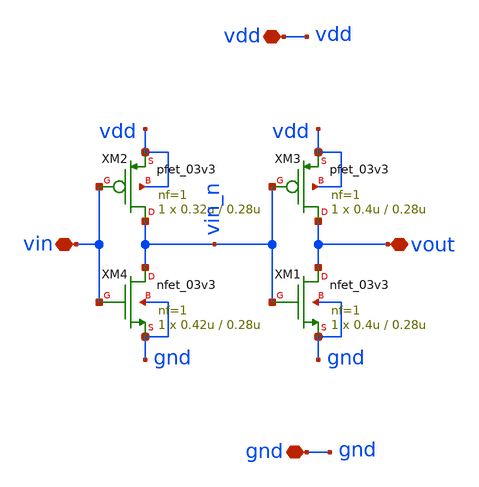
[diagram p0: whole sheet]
** sch_path: designs/libs/core_buffer/buffer.sch
**.subckt buffer vdd gnd vout vin
*.iopin vdd
*.iopin gnd
*.iopin vout
*.iopin vin
XM2 vin_n vin vdd vdd pfet_03v3 L=0.28u W=0.32u nf=1 ad='int((nf+1)/2) * W/nf * 0.18u' as='int((nf+2)/2) * W/nf * 0.18u'
+ pd='2*int((nf+1)/2) * (W/nf + 0.18u)' ps='2*int((nf+2)/2) * (W/nf + 0.18u)' nrd='0.18u / W' nrs='0.18u / W'
+ sa=0 sb=0 sd=0 m=1
XM4 vin_n vin gnd gnd nfet_03v3 L=0.28u W=0.42u nf=1 ad='int((nf+1)/2) * W/nf * 0.18u' as='int((nf+2)/2) * W/nf * 0.18u'
+ pd='2*int((nf+1)/2) * (W/nf + 0.18u)' ps='2*int((nf+2)/2) * (W/nf + 0.18u)' nrd='0.18u / W' nrs='0.18u / W'
+ sa=0 sb=0 sd=0 m=1
XM1 vout vin_n gnd gnd nfet_03v3 L=0.28u W=0.4u nf=1 ad='int((nf+1)/2) * W/nf * 0.18u' as='int((nf+2)/2) * W/nf * 0.18u'
+ pd='2*int((nf+1)/2) * (W/nf + 0.18u)' ps='2*int((nf+2)/2) * (W/nf + 0.18u)' nrd='0.18u / W' nrs='0.18u / W'
+ sa=0 sb=0 sd=0 m=1
XM3 vout vin_n vdd vdd pfet_03v3 L=0.28u W=0.4u nf=1 ad='int((nf+1)/2) * W/nf * 0.18u' as='int((nf+2)/2) * W/nf * 0.18u'
+ pd='2*int((nf+1)/2) * (W/nf + 0.18u)' ps='2*int((nf+2)/2) * (W/nf + 0.18u)' nrd='0.18u / W' nrs='0.18u / W'
+ sa=0 sb=0 sd=0 m=1
**.ends
.end
